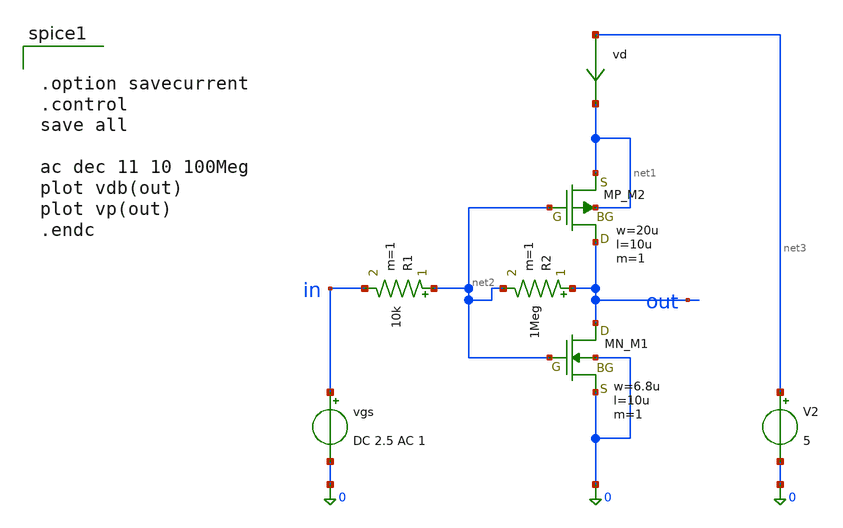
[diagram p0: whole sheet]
** sch_path: member_project/JJY_Receiver/Masahiro/jjy_recv/pre_amp/inverter_sim_ac.sch
**.subckt inverter_sim_ac
XM1 out net2 0 0 NMOS w=6.8u l=10u as=0 ad=0 ps=0 pd=0 nrd=0 nrs=0 m=1
XM2 out net2 net1 net1 PMOS w=20u l=10u as=0 ad=0 ps=0 pd=0 nrd=0 nrs=0 m=1
vgs in 0 DC 2.5 AC 1
V2 net3 0 5
vd net3 net1 0
.save i(vd)
R2 out net2 1Meg m=1
R1 net2 in 10k m=1
**** begin user architecture code
 .include $::LIB/ip62_models


.option savecurrent
.control
save all

ac dec 11 10 100Meg
plot vdb(out)
plot vp(out)
.endc


**** end user architecture code
**.ends
.end
